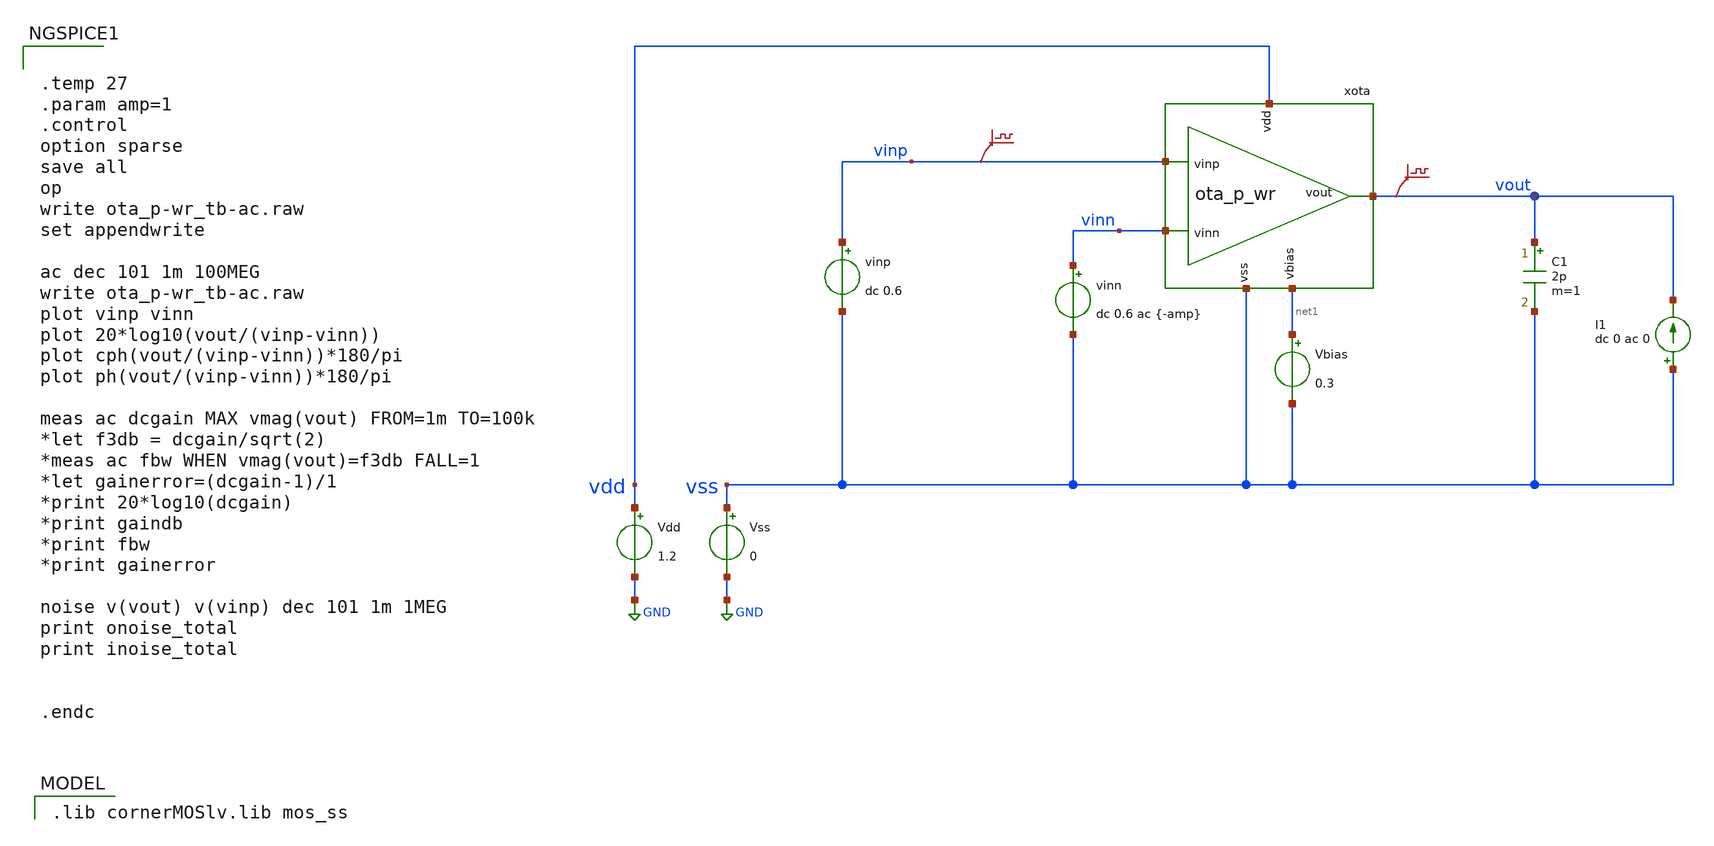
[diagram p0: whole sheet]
** sch_path: v2_feature_extr/ota_p-wr_tb-ac.sch
* (c) 2024-2025 Harald Pretl, Apache-2.0 license
**.subckt ota_p-wr_tb-ac
Vdd vdd GND 1.2
xota vdd vout vinp vinn net1 vss ota_p_wr
Vss vss GND 0
C1 vout vss 2p m=1
.save v(vinp)
.save v(vout)
I1 vss vout dc 0 ac 0
vinn vinn vss dc 0.6 ac {-amp}
Vbias net1 vss 0.3
vinp vinp vss dc 0.6
**** begin user architecture code
 .lib cornerMOSlv.lib mos_ss



.temp 27
.param amp=1
.control
option sparse
save all
op
write ota_p-wr_tb-ac.raw
set appendwrite

ac dec 101 1m 100MEG
write ota_p-wr_tb-ac.raw
plot vinp vinn
plot 20*log10(vout/(vinp-vinn))
plot cph(vout/(vinp-vinn))*180/pi
plot ph(vout/(vinp-vinn))*180/pi

meas ac dcgain MAX vmag(vout) FROM=1m TO=100k
*let f3db = dcgain/sqrt(2)
*meas ac fbw WHEN vmag(vout)=f3db FALL=1
*let gainerror=(dcgain-1)/1
*print 20*log10(dcgain)
*print gaindb
*print fbw
*print gainerror

noise v(vout) v(vinp) dec 101 1m 1MEG
print onoise_total
print inoise_total


.endc


**** end user architecture code
**.ends
.GLOBAL GND
.end
